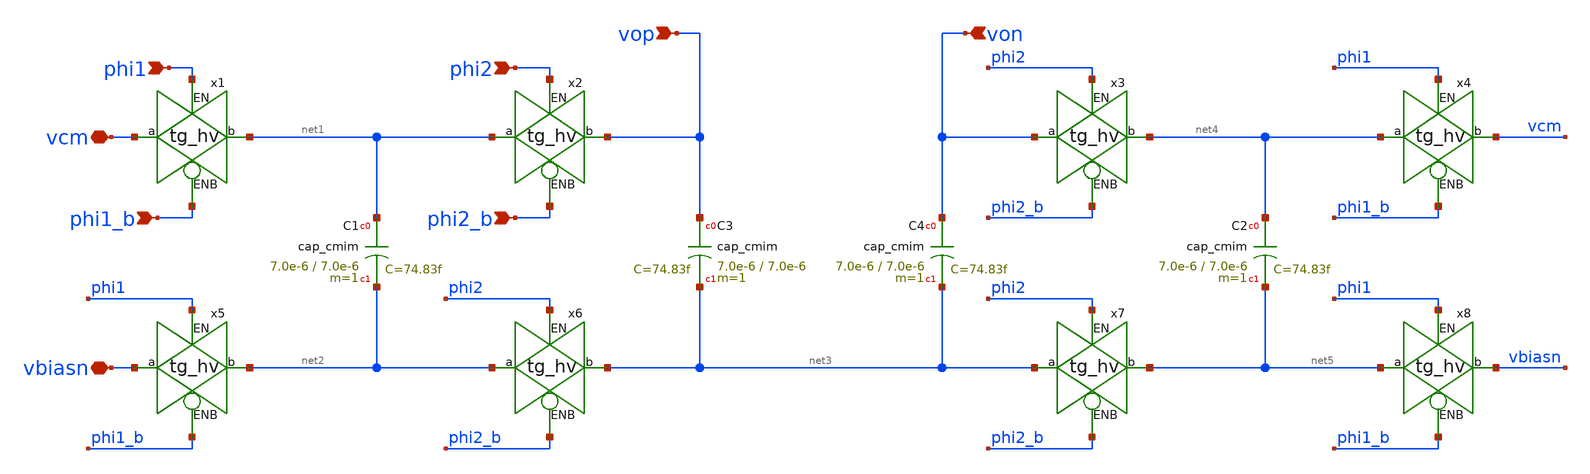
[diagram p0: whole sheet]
** sch_path: 3_real_circuits/sc_cmfb.sch
**.subckt sc_cmfb vop von phi1 phi1_b vcm phi2 phi2_b vbiasn
*.ipin vop
*.ipin von
*.ipin phi1
*.ipin phi1_b
*.iopin vcm
*.ipin phi2
*.ipin phi2_b
*.iopin vbiasn
XC1 net1 net2 cap_cmim w=7.0e-6 l=7.0e-6 m=1 mm_ok=1
XC3 vop net3 cap_cmim w=7.0e-6 l=7.0e-6 m=1 mm_ok=1
x2 phi2_b phi2 net1 vop tg_hv
x1 phi1_b phi1 vcm net1 tg_hv
XC2 net4 net5 cap_cmim w=7.0e-6 l=7.0e-6 m=1 mm_ok=1
x3 phi2_b phi2 von net4 tg_hv
x4 phi1_b phi1 net4 vcm tg_hv
x5 phi1_b phi1 vbiasn net2 tg_hv
x6 phi2_b phi2 net2 net3 tg_hv
x7 phi2_b phi2 net3 net5 tg_hv
x8 phi1_b phi1 net5 vbiasn tg_hv
XC4 von net3 cap_cmim w=7.0e-6 l=7.0e-6 m=1 mm_ok=1
**.ends

* expanding   symbol:  tg_hv.sym # of pins=4
** sym_path: 3_real_circuits/tg_hv.sym
** sch_path: 3_real_circuits/tg_hv.sch
.subckt tg_hv ENB EN a b
*.ipin ENB
*.ipin EN
*.iopin b
*.iopin a
XM2 a ENB b vdd sg13_hv_pmos w=10u l=0.45u ng=1 m=1 mm_ok=1
XM1 a EN b GND sg13_hv_nmos w=5u l=0.45u ng=1 m=1 mm_ok=1
.ends

.GLOBAL vdd
.GLOBAL GND
.end
